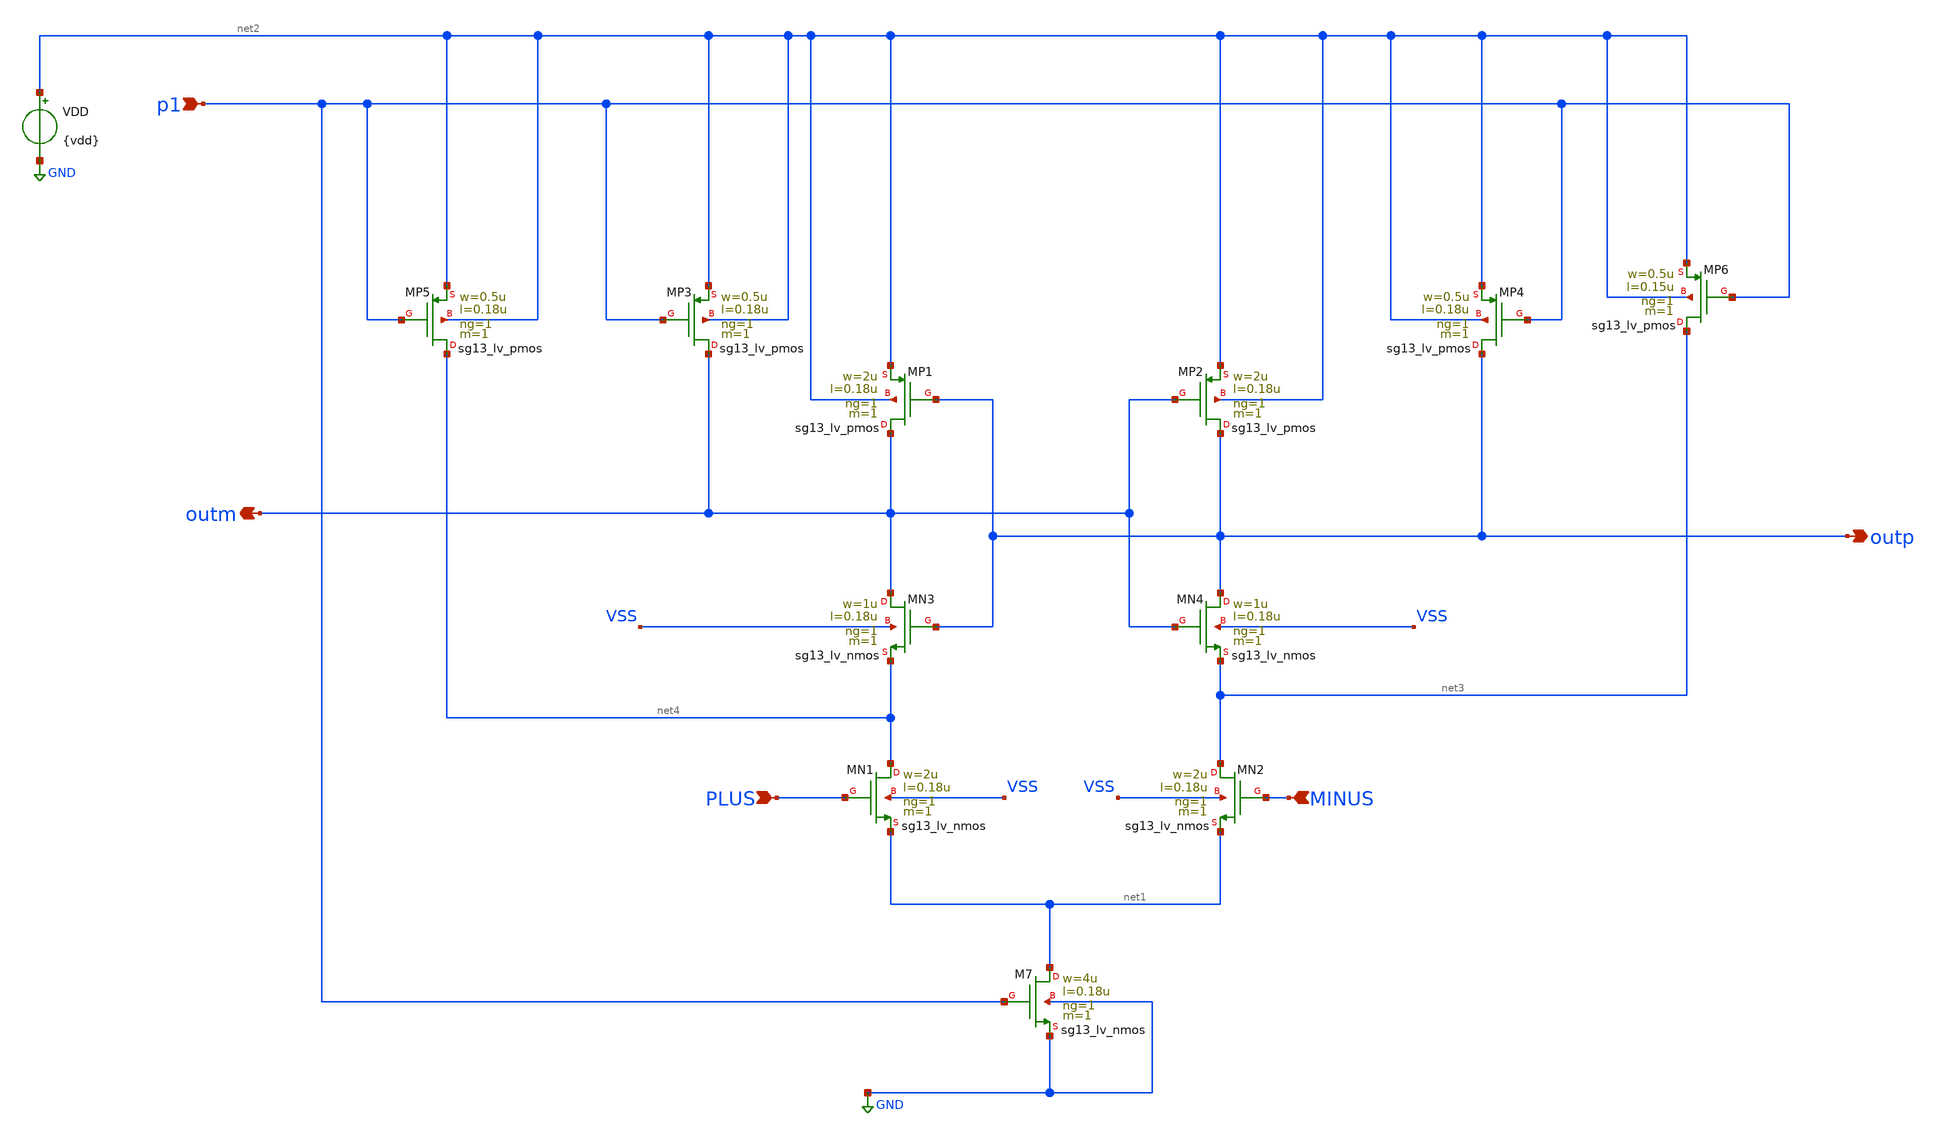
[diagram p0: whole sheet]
** sch_path: DSM/Schematics/Sneha/Comp_Test-3.sch
**.subckt Comp_Test-3 PLUS MINUS p1 outp outm
*.ipin PLUS
*.ipin MINUS
*.ipin p1
*.opin outp
*.opin outm
XMN3 outm outp net4 VSS sg13_lv_nmos w=1u l=0.18u ng=1 m=1 mm_ok=1
XMP5 net4 p1 net2 net2 sg13_lv_pmos w=0.5u l=0.18u ng=1 m=1 mm_ok=1
XMP3 outm p1 net2 net2 sg13_lv_pmos w=0.5u l=0.18u ng=1 m=1 mm_ok=1
XMP1 outm outp net2 net2 sg13_lv_pmos w=2u l=0.18u ng=1 m=1 mm_ok=1
XMP2 outp outm net2 net2 sg13_lv_pmos w=2u l=0.18u ng=1 m=1 mm_ok=1
XMP4 outp p1 net2 net2 sg13_lv_pmos w=0.5u l=0.18u ng=1 m=1 mm_ok=1
XMP6 net3 p1 net2 net2 sg13_lv_pmos w=0.5u l=0.15u ng=1 m=1 mm_ok=1
XMN4 outp outm net3 VSS sg13_lv_nmos w=1u l=0.18u ng=1 m=1 mm_ok=1
XMN1 net4 PLUS net1 VSS sg13_lv_nmos w=2u l=0.18u ng=1 m=1 mm_ok=1
XMN2 net3 MINUS net1 VSS sg13_lv_nmos w=2u l=0.18u ng=1 m=1 mm_ok=1
XM7 net1 p1 GND GND sg13_lv_nmos w=4u l=0.18u ng=1 m=1 mm_ok=1
VDD net2 GND {vdd}
**.ends
.GLOBAL GND
.end
